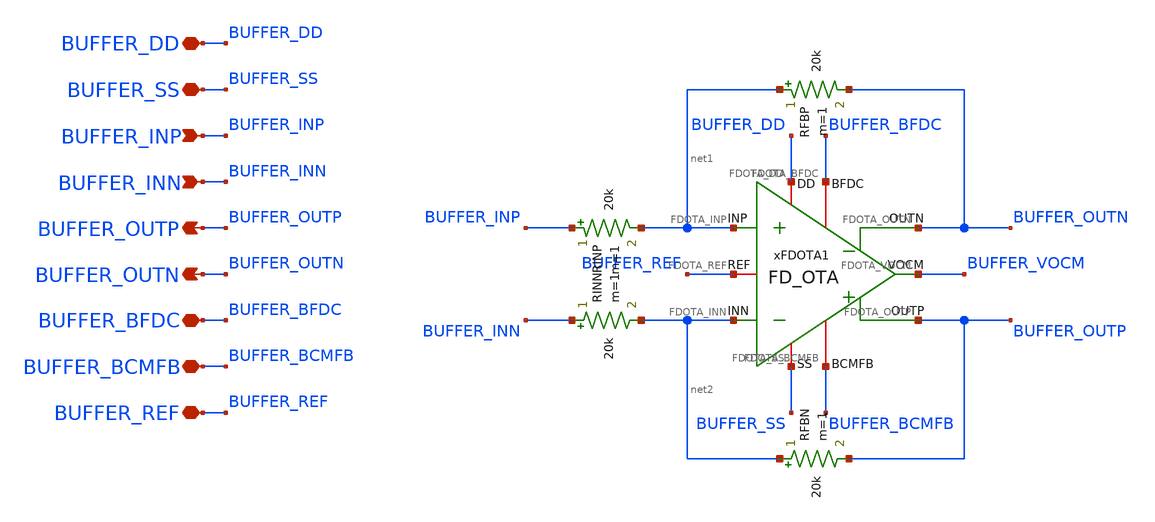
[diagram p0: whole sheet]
** sch_path: Design_Files/IC Design/Schematic/BUFFER/BUFFER.sch
**.subckt BUFFER BUFFER_DD BUFFER_SS BUFFER_INP BUFFER_INN BUFFER_OUTP BUFFER_BFDC BUFFER_OUTN
*+ BUFFER_BCMFB BUFFER_REF
*.iopin BUFFER_DD
*.iopin BUFFER_SS
*.ipin BUFFER_INP
*.ipin BUFFER_INN
*.opin BUFFER_OUTP
*.iopin BUFFER_BFDC
*.opin BUFFER_OUTN
*.iopin BUFFER_BCMFB
*.iopin BUFFER_REF
RFBP net1 BUFFER_OUTN 20k m=1
xFDOTA1 BUFFER_DD BUFFER_SS net1 net2 BUFFER_OUTN BUFFER_BFDC BUFFER_OUTP BUFFER_BCMFB BUFFER_REF
+ BUFFER_VOCM FD_OTA
RINN BUFFER_INN net2 20k m=1
RINP BUFFER_INP net1 20k m=1
RFBN net2 BUFFER_OUTP 20k m=1
**.ends

* expanding   symbol:  ECG_Acquisition_IC/Design_Files/IC Design/Schematic/FD_OTA/FDOTA/FD_OTA.sym #
*+ of pins=10
** sym_path: Design_Files/IC Design/Schematic/FD_OTA/FDOTA/FD_OTA.sym
** sch_path: Design_Files/IC Design/Schematic/FD_OTA/FDOTA/FD_OTA.sch
.subckt FD_OTA FDOTA_DD FDOTA_SS FDOTA_INP FDOTA_INN FDOTA_OUTN FDOTA_BFDC FDOTA_OUTP FDOTA_BCMFB
+ FDOTA_REF FDOTA_VOCM
*.iopin FDOTA_DD
*.iopin FDOTA_SS
*.ipin FDOTA_INP
*.ipin FDOTA_INN
*.opin FDOTA_OUTP
*.iopin FDOTA_BFDC
*.opin FDOTA_OUTN
*.iopin FDOTA_BCMFB
*.iopin FDOTA_REF
*.iopin FDOTA_VOCM
R1 FDOTA_OUTP FDOTA_VOCM 100k m=1
R2 FDOTA_VOCM FDOTA_OUTN 100k m=1
C1 FDOTA_OUTP FDOTA_VOCM 50f m=1
C2 FDOTA_VOCM FDOTA_OUTN 50f m=1
xFDC1 FDOTA_DD FDOTA_SS FDOTA_INP FDOTA_INN FDOTA_OUTN FDOTA_BFDC FDOTA_OUTP FDOTA_VCMFB FDC
xCMFB1 FDOTA_DD FDOTA_SS FDOTA_VOCM FDOTA_REF FDOTA_VCMFB FDOTA_BCMFB CMFB
.ends


* expanding   symbol:  ECG_Acquisition_IC/Design_Files/IC Design/Schematic/FD_OTA/FDC/FDC.sym # of
*+ pins=8
** sym_path: Design_Files/IC Design/Schematic/FD_OTA/FDC/FDC.sym
** sch_path: Design_Files/IC Design/Schematic/FD_OTA/FDC/FDC.sch
.subckt FDC FDC_DD FDC_SS FDC_INP FDC_INN FDC_OUTN FDC_B FDC_OUTP FDC_CMFB
*.iopin FDC_DD
*.iopin FDC_SS
*.ipin FDC_INP
*.ipin FDC_INN
*.opin FDC_OUTP
*.iopin FDC_B
*.opin FDC_OUTN
*.iopin FDC_CMFB
XM3 net4 FDC_CMFB FDC_DD FDC_DD pfet_03v3 L=2u W=1u nf=1 ad='int((nf+1)/2) * W/nf * 0.18u' as='int((nf+2)/2) * W/nf * 0.18u'
+ pd='2*int((nf+1)/2) * (W/nf + 0.18u)' ps='2*int((nf+2)/2) * (W/nf + 0.18u)' nrd='0.18u / W' nrs='0.18u / W'
+ sa=0 sb=0 sd=0 m=200
XM8 FDC_OUTP FDC_B FDC_SS FDC_SS nfet_03v3 L=0.5u W=1u nf=1 ad='int((nf+1)/2) * W/nf * 0.18u' as='int((nf+2)/2) * W/nf * 0.18u'
+ pd='2*int((nf+1)/2) * (W/nf + 0.18u)' ps='2*int((nf+2)/2) * (W/nf + 0.18u)' nrd='0.18u / W' nrs='0.18u / W'
+ sa=0 sb=0 sd=0 m=100
Rz net1 net2 3.5k m=1
XM5 net3 FDC_B FDC_SS FDC_SS nfet_03v3 L=2u W=1u nf=1 ad='int((nf+1)/2) * W/nf * 0.18u' as='int((nf+2)/2) * W/nf * 0.18u'
+ pd='2*int((nf+1)/2) * (W/nf + 0.18u)' ps='2*int((nf+2)/2) * (W/nf + 0.18u)' nrd='0.18u / W' nrs='0.18u / W'
+ sa=0 sb=0 sd=0 m=10
XM6 FDC_OUTP net1 FDC_DD FDC_DD pfet_03v3 L=0.5u W=1u nf=1 ad='int((nf+1)/2) * W/nf * 0.18u' as='int((nf+2)/2) * W/nf * 0.18u'
+ pd='2*int((nf+1)/2) * (W/nf + 0.18u)' ps='2*int((nf+2)/2) * (W/nf + 0.18u)' nrd='0.18u / W' nrs='0.18u / W'
+ sa=0 sb=0 sd=0 m=200
XM10 FDC_B FDC_B FDC_SS FDC_SS nfet_03v3 L=2u W=1u nf=1 ad='int((nf+1)/2) * W/nf * 0.18u' as='int((nf+2)/2) * W/nf * 0.18u'
+ pd='2*int((nf+1)/2) * (W/nf + 0.18u)' ps='2*int((nf+2)/2) * (W/nf + 0.18u)' nrd='0.18u / W' nrs='0.18u / W'
+ sa=0 sb=0 sd=0 m=20
Cc net2 FDC_OUTP 2.5p m=1
XM9 FDC_OUTN FDC_B FDC_SS FDC_SS nfet_03v3 L=0.5u W=1u nf=1 ad='int((nf+1)/2) * W/nf * 0.18u' as='int((nf+2)/2) * W/nf * 0.18u'
+ pd='2*int((nf+1)/2) * (W/nf + 0.18u)' ps='2*int((nf+2)/2) * (W/nf + 0.18u)' nrd='0.18u / W' nrs='0.18u / W'
+ sa=0 sb=0 sd=0 m=100
Rz1 net4 net5 3.5k m=1
XM7 FDC_OUTN net4 FDC_DD FDC_DD pfet_03v3 L=0.5u W=1u nf=1 ad='int((nf+1)/2) * W/nf * 0.18u' as='int((nf+2)/2) * W/nf * 0.18u'
+ pd='2*int((nf+1)/2) * (W/nf + 0.18u)' ps='2*int((nf+2)/2) * (W/nf + 0.18u)' nrd='0.18u / W' nrs='0.18u / W'
+ sa=0 sb=0 sd=0 m=200
Cc1 net5 FDC_OUTN 2.5p m=1
XM4 net1 FDC_CMFB FDC_DD FDC_DD pfet_03v3 L=2u W=1u nf=1 ad='int((nf+1)/2) * W/nf * 0.18u' as='int((nf+2)/2) * W/nf * 0.18u'
+ pd='2*int((nf+1)/2) * (W/nf + 0.18u)' ps='2*int((nf+2)/2) * (W/nf + 0.18u)' nrd='0.18u / W' nrs='0.18u / W'
+ sa=0 sb=0 sd=0 m=200
XM1 net4 FDC_INN net3 FDC_SS nfet_03v3 L=2u W=1u nf=1 ad='int((nf+1)/2) * W/nf * 0.18u' as='int((nf+2)/2) * W/nf * 0.18u'
+ pd='2*int((nf+1)/2) * (W/nf + 0.18u)' ps='2*int((nf+2)/2) * (W/nf + 0.18u)' nrd='0.18u / W' nrs='0.18u / W'
+ sa=0 sb=0 sd=0 m=200
XM2 net1 FDC_INP net3 FDC_SS nfet_03v3 L=2u W=1u nf=1 ad='int((nf+1)/2) * W/nf * 0.18u' as='int((nf+2)/2) * W/nf * 0.18u'
+ pd='2*int((nf+1)/2) * (W/nf + 0.18u)' ps='2*int((nf+2)/2) * (W/nf + 0.18u)' nrd='0.18u / W' nrs='0.18u / W'
+ sa=0 sb=0 sd=0 m=200
.ends


* expanding   symbol:  ECG_Acquisition_IC/Design_Files/IC Design/Schematic/FD_OTA/CMFB/CMFB.sym # of
*+ pins=6
** sym_path: Design_Files/IC Design/Schematic/FD_OTA/CMFB/CMFB.sym
** sch_path: Design_Files/IC Design/Schematic/FD_OTA/CMFB/CMFB.sch
.subckt CMFB CMFB_DD CMFB_SS CMFB_IN CMFB_REF CMFB_OUT CMFB_B
*.iopin CMFB_DD
*.iopin CMFB_SS
*.ipin CMFB_IN
*.ipin CMFB_REF
*.opin CMFB_OUT
*.iopin CMFB_B
XM4 CMFB_OUT CMFB_OUT CMFB_DD CMFB_DD pfet_03v3 L=0.5u W=1u nf=1 ad='int((nf+1)/2) * W/nf * 0.18u' as='int((nf+2)/2) * W/nf * 0.18u'
+ pd='2*int((nf+1)/2) * (W/nf + 0.18u)' ps='2*int((nf+2)/2) * (W/nf + 0.18u)' nrd='0.18u / W' nrs='0.18u / W'
+ sa=0 sb=0 sd=0 m=77
XM3 net2 net2 CMFB_DD CMFB_DD pfet_03v3 L=0.5u W=1u nf=1 ad='int((nf+1)/2) * W/nf * 0.18u' as='int((nf+2)/2) * W/nf * 0.18u'
+ pd='2*int((nf+1)/2) * (W/nf + 0.18u)' ps='2*int((nf+2)/2) * (W/nf + 0.18u)' nrd='0.18u / W' nrs='0.18u / W'
+ sa=0 sb=0 sd=0 m=77
XM1 net2 CMFB_REF net1 CMFB_SS nfet_03v3 L=0.5u W=1u nf=1 ad='int((nf+1)/2) * W/nf * 0.18u' as='int((nf+2)/2) * W/nf * 0.18u'
+ pd='2*int((nf+1)/2) * (W/nf + 0.18u)' ps='2*int((nf+2)/2) * (W/nf + 0.18u)' nrd='0.18u / W' nrs='0.18u / W'
+ sa=0 sb=0 sd=0 m=5
XM2 CMFB_OUT CMFB_IN net1 CMFB_SS nfet_03v3 L=0.5u W=1u nf=1 ad='int((nf+1)/2) * W/nf * 0.18u' as='int((nf+2)/2) * W/nf * 0.18u'
+ pd='2*int((nf+1)/2) * (W/nf + 0.18u)' ps='2*int((nf+2)/2) * (W/nf + 0.18u)' nrd='0.18u / W' nrs='0.18u / W'
+ sa=0 sb=0 sd=0 m=5
XM5 net1 CMFB_B CMFB_SS CMFB_SS nfet_03v3 L=2u W=1u nf=1 ad='int((nf+1)/2) * W/nf * 0.18u' as='int((nf+2)/2) * W/nf * 0.18u'
+ pd='2*int((nf+1)/2) * (W/nf + 0.18u)' ps='2*int((nf+2)/2) * (W/nf + 0.18u)' nrd='0.18u / W' nrs='0.18u / W'
+ sa=0 sb=0 sd=0 m=20
XM10 CMFB_B CMFB_B CMFB_SS CMFB_SS nfet_03v3 L=2u W=1u nf=1 ad='int((nf+1)/2) * W/nf * 0.18u' as='int((nf+2)/2) * W/nf * 0.18u'
+ pd='2*int((nf+1)/2) * (W/nf + 0.18u)' ps='2*int((nf+2)/2) * (W/nf + 0.18u)' nrd='0.18u / W' nrs='0.18u / W'
+ sa=0 sb=0 sd=0 m=20
.ends

.end
